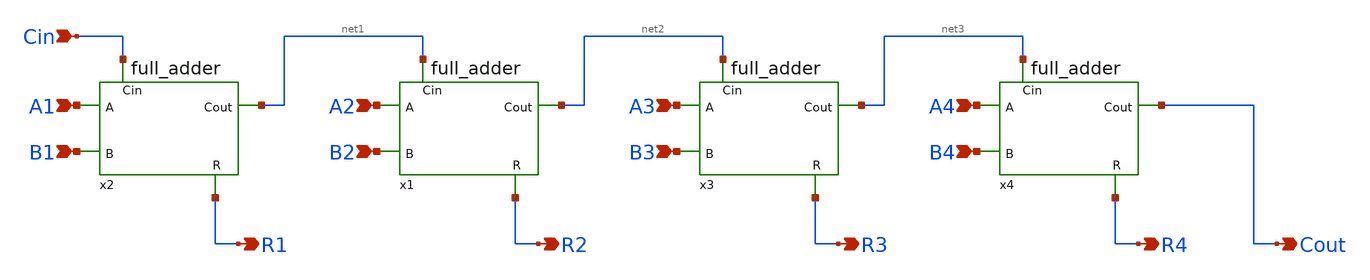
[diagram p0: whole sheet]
** sch_path: Circuiti/adders/4bit_adder.sch
**.subckt 4bit_adder A1 B1 A2 B2 A3 B3 A4 B4 R1 R2 R3 R4 Cout Cin
*.ipin A1
*.ipin B1
*.ipin A2
*.ipin B2
*.ipin A3
*.ipin B3
*.ipin A4
*.ipin B4
*.opin R1
*.opin R2
*.opin R3
*.opin R4
*.opin Cout
*.ipin Cin
x2 A1 B1 R1 Cin net1 full_adder
x1 A2 B2 R2 net1 net2 full_adder
x3 A3 B3 R3 net2 net3 full_adder
x4 A4 B4 R4 net3 Cout full_adder
**.ends
.end
